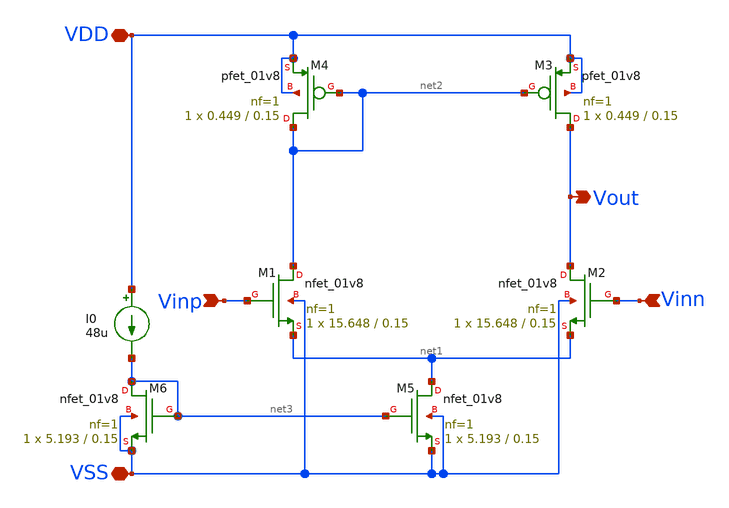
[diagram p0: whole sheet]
** sch_path: opamp_design/simple_one_stage_opamp/simple_one_stage_opamp.sch
**.subckt simple_one_stage_opamp VSS VDD Vinp Vinn Vout
*.iopin VSS
*.iopin VDD
*.ipin Vinp
*.ipin Vinn
*.opin Vout
XM1 net2 Vinp net1 VSS sky130_fd_pr__nfet_01v8 L=0.15 W=15.648 nf=1 ad='int((nf+1)/2) * W/nf * 0.29'
+ as='int((nf+2)/2) * W/nf * 0.29' pd='2*int((nf+1)/2) * (W/nf + 0.29)' ps='2*int((nf+2)/2) * (W/nf + 0.29)'
+ nrd='0.29 / W' nrs='0.29 / W' sa=0 sb=0 sd=0 mult=1 m=1
XM4 net2 net2 VDD VDD sky130_fd_pr__pfet_01v8 L=0.15 W=0.449 nf=1 ad='int((nf+1)/2) * W/nf * 0.29' as='int((nf+2)/2) * W/nf * 0.29'
+ pd='2*int((nf+1)/2) * (W/nf + 0.29)' ps='2*int((nf+2)/2) * (W/nf + 0.29)' nrd='0.29 / W' nrs='0.29 / W'
+ sa=0 sb=0 sd=0 mult=1 m=1
XM2 Vout Vinn net1 VSS sky130_fd_pr__nfet_01v8 L=0.15 W=15.648 nf=1 ad='int((nf+1)/2) * W/nf * 0.29'
+ as='int((nf+2)/2) * W/nf * 0.29' pd='2*int((nf+1)/2) * (W/nf + 0.29)' ps='2*int((nf+2)/2) * (W/nf + 0.29)'
+ nrd='0.29 / W' nrs='0.29 / W' sa=0 sb=0 sd=0 mult=1 m=1
XM3 Vout net2 VDD VDD sky130_fd_pr__pfet_01v8 L=0.15 W=0.449 nf=1 ad='int((nf+1)/2) * W/nf * 0.29' as='int((nf+2)/2) * W/nf * 0.29'
+ pd='2*int((nf+1)/2) * (W/nf + 0.29)' ps='2*int((nf+2)/2) * (W/nf + 0.29)' nrd='0.29 / W' nrs='0.29 / W'
+ sa=0 sb=0 sd=0 mult=1 m=1
XM5 net1 net3 VSS VSS sky130_fd_pr__nfet_01v8 L=0.15 W=5.193 nf=1 ad='int((nf+1)/2) * W/nf * 0.29' as='int((nf+2)/2) * W/nf * 0.29'
+ pd='2*int((nf+1)/2) * (W/nf + 0.29)' ps='2*int((nf+2)/2) * (W/nf + 0.29)' nrd='0.29 / W' nrs='0.29 / W'
+ sa=0 sb=0 sd=0 mult=1 m=1
XM6 net3 net3 VSS VSS sky130_fd_pr__nfet_01v8 L=0.15 W=5.193 nf=1 ad='int((nf+1)/2) * W/nf * 0.29' as='int((nf+2)/2) * W/nf * 0.29'
+ pd='2*int((nf+1)/2) * (W/nf + 0.29)' ps='2*int((nf+2)/2) * (W/nf + 0.29)' nrd='0.29 / W' nrs='0.29 / W'
+ sa=0 sb=0 sd=0 mult=1 m=1
I0 VDD net3 48u
**.ends
.end
